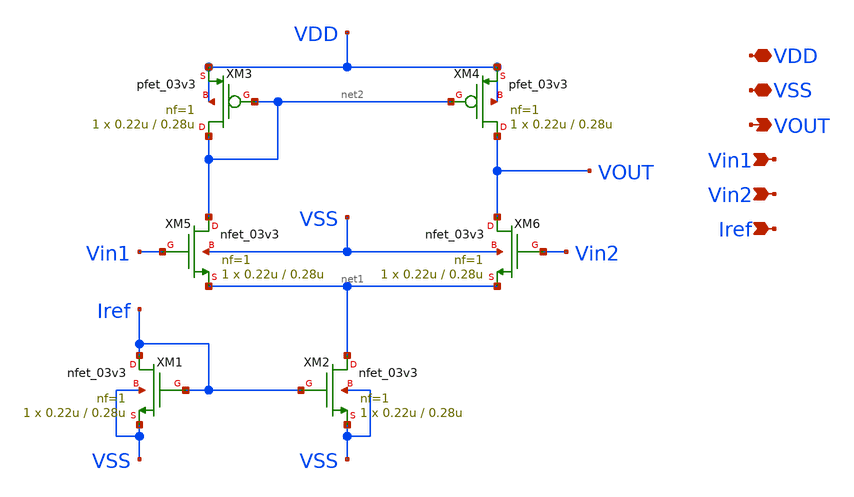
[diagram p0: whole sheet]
** sch_path: week02_current_diffpair/tugas5_cascode_current_mirror/nmos-ota.sch
**.subckt nmos-ota VDD VSS VOUT Vin1 Vin2 Iref
*.iopin VDD
*.iopin VSS
*.opin VOUT
*.ipin Vin1
*.ipin Vin2
*.ipin Iref
XM1 Iref Iref VSS VSS nfet_03v3 L=0.28u W=0.22u nf=1 ad='int((nf+1)/2) * W/nf * 0.18u' as='int((nf+2)/2) * W/nf * 0.18u'
+ pd='2*int((nf+1)/2) * (W/nf + 0.18u)' ps='2*int((nf+2)/2) * (W/nf + 0.18u)' nrd='0.18u / W' nrs='0.18u / W'
+ sa=0 sb=0 sd=0 m=1
XM2 net1 Iref VSS VSS nfet_03v3 L=0.28u W=0.22u nf=1 ad='int((nf+1)/2) * W/nf * 0.18u' as='int((nf+2)/2) * W/nf * 0.18u'
+ pd='2*int((nf+1)/2) * (W/nf + 0.18u)' ps='2*int((nf+2)/2) * (W/nf + 0.18u)' nrd='0.18u / W' nrs='0.18u / W'
+ sa=0 sb=0 sd=0 m=1
XM3 net2 net2 VDD VDD pfet_03v3 L=0.28u W=0.22u nf=1 ad='int((nf+1)/2) * W/nf * 0.18u' as='int((nf+2)/2) * W/nf * 0.18u'
+ pd='2*int((nf+1)/2) * (W/nf + 0.18u)' ps='2*int((nf+2)/2) * (W/nf + 0.18u)' nrd='0.18u / W' nrs='0.18u / W'
+ sa=0 sb=0 sd=0 m=1
XM4 VOUT net2 VDD VDD pfet_03v3 L=0.28u W=0.22u nf=1 ad='int((nf+1)/2) * W/nf * 0.18u' as='int((nf+2)/2) * W/nf * 0.18u'
+ pd='2*int((nf+1)/2) * (W/nf + 0.18u)' ps='2*int((nf+2)/2) * (W/nf + 0.18u)' nrd='0.18u / W' nrs='0.18u / W'
+ sa=0 sb=0 sd=0 m=1
XM5 net2 Vin1 net1 VSS nfet_03v3 L=0.28u W=0.22u nf=1 ad='int((nf+1)/2) * W/nf * 0.18u' as='int((nf+2)/2) * W/nf * 0.18u'
+ pd='2*int((nf+1)/2) * (W/nf + 0.18u)' ps='2*int((nf+2)/2) * (W/nf + 0.18u)' nrd='0.18u / W' nrs='0.18u / W'
+ sa=0 sb=0 sd=0 m=1
XM6 VOUT Vin2 net1 VSS nfet_03v3 L=0.28u W=0.22u nf=1 ad='int((nf+1)/2) * W/nf * 0.18u' as='int((nf+2)/2) * W/nf * 0.18u'
+ pd='2*int((nf+1)/2) * (W/nf + 0.18u)' ps='2*int((nf+2)/2) * (W/nf + 0.18u)' nrd='0.18u / W' nrs='0.18u / W'
+ sa=0 sb=0 sd=0 m=1
**.ends
.end
